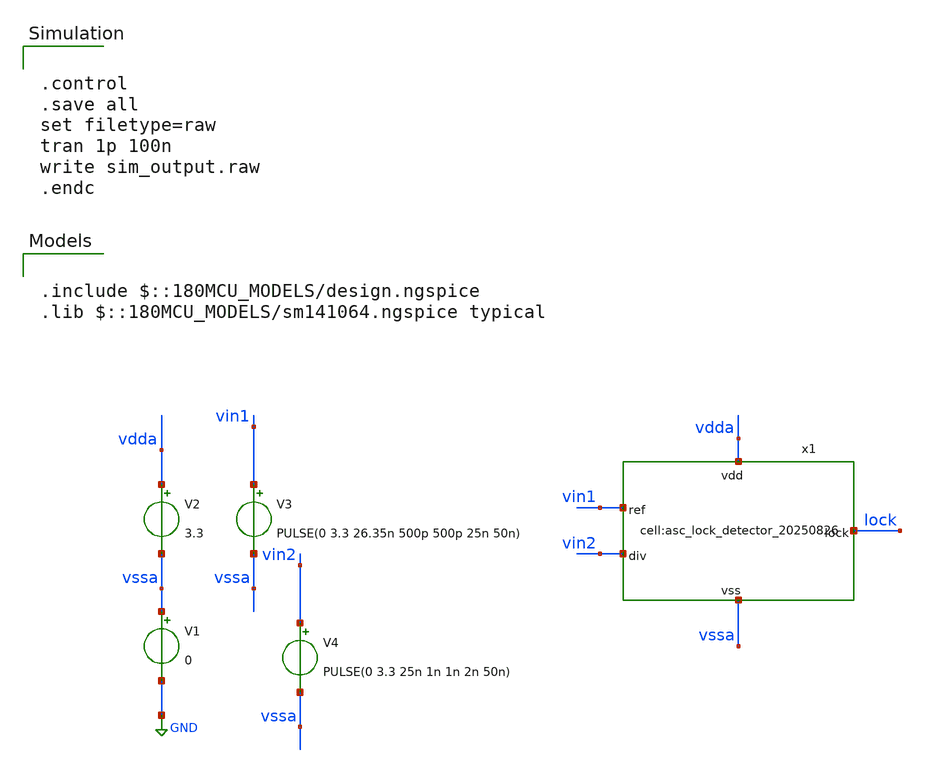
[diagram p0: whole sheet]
** sch_path: designs/libs/tb_analog/tb_asc_lock_detector_20250826/tb_asc_lock_detector_20250826.sch
**.subckt tb_asc_lock_detector_20250826
V1 vssa GND 0
V2 vdda vssa 3.3
V3 vin1 vssa PULSE(0 3.3 26.35n 500p 500p 25n 50n)
V4 vin2 vssa PULSE(0 3.3 25n 1n 1n 2n 50n)
x1 vdda lock vssa vin2 vin1 asc_lock_detector_20250826
**** begin user architecture code

.include $::180MCU_MODELS/design.ngspice
.lib $::180MCU_MODELS/sm141064.ngspice typical



.control
.save all
set filetype=raw
tran 1p 100n
write sim_output.raw
.endc


**** end user architecture code
**.ends
.GLOBAL GND
.end
